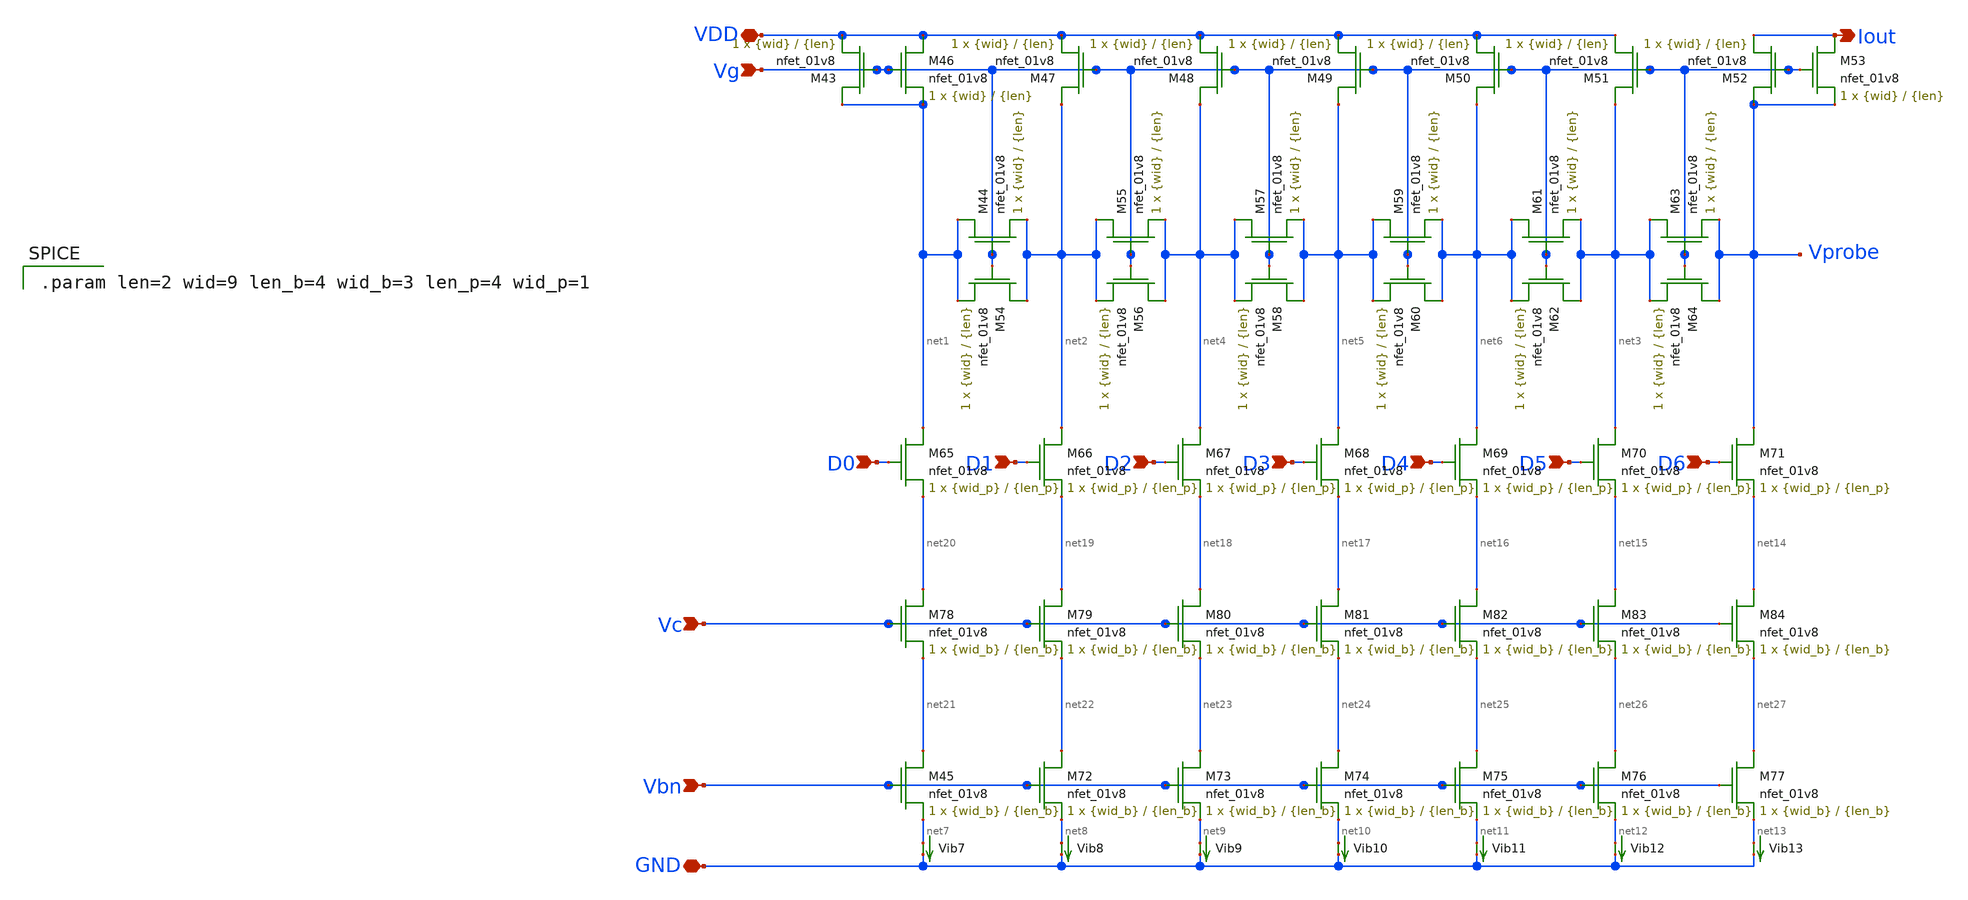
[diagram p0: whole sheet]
** sch_path: mp3/ladder.sch
**.subckt ladder Vbn VDD Iout GND D0 D1 D2 D3 D4 D5 D6 Vg Vc
*.ipin Vbn
*.iopin VDD
*.opin Iout
*.iopin GND
*.ipin D0
*.ipin D1
*.ipin D2
*.ipin D3
*.ipin D4
*.ipin D5
*.ipin D6
*.ipin Vg
*.ipin Vc
XM43 net1 Vg VDD GND sky130_fd_pr__nfet_01v8 L={len} W={wid} nf=1 ad='int((nf+1)/2) * W/nf * 0.29' as='int((nf+2)/2) * W/nf * 0.29'
+ pd='2*int((nf+1)/2) * (W/nf + 0.29)' ps='2*int((nf+2)/2) * (W/nf + 0.29)' nrd='0.29 / W' nrs='0.29 / W'
+ sa=0 sb=0 sd=0 mult=1 m=1
XM44 net1 Vg net2 GND sky130_fd_pr__nfet_01v8 L={len} W={wid} nf=1 ad='int((nf+1)/2) * W/nf * 0.29' as='int((nf+2)/2) * W/nf * 0.29'
+ pd='2*int((nf+1)/2) * (W/nf + 0.29)' ps='2*int((nf+2)/2) * (W/nf + 0.29)' nrd='0.29 / W' nrs='0.29 / W'
+ sa=0 sb=0 sd=0 mult=1 m=1
XM45 net21 Vbn net7 GND sky130_fd_pr__nfet_01v8 L={len_b} W={wid_b} nf=1 ad='int((nf+1)/2) * W/nf * 0.29'
+ as='int((nf+2)/2) * W/nf * 0.29' pd='2*int((nf+1)/2) * (W/nf + 0.29)' ps='2*int((nf+2)/2) * (W/nf + 0.29)'
+ nrd='0.29 / W' nrs='0.29 / W' sa=0 sb=0 sd=0 mult=1 m=1
XM46 VDD Vg net1 GND sky130_fd_pr__nfet_01v8 L={len} W={wid} nf=1 ad='int((nf+1)/2) * W/nf * 0.29' as='int((nf+2)/2) * W/nf * 0.29'
+ pd='2*int((nf+1)/2) * (W/nf + 0.29)' ps='2*int((nf+2)/2) * (W/nf + 0.29)' nrd='0.29 / W' nrs='0.29 / W'
+ sa=0 sb=0 sd=0 mult=1 m=1
XM47 net2 Vg VDD GND sky130_fd_pr__nfet_01v8 L={len} W={wid} nf=1 ad='int((nf+1)/2) * W/nf * 0.29' as='int((nf+2)/2) * W/nf * 0.29'
+ pd='2*int((nf+1)/2) * (W/nf + 0.29)' ps='2*int((nf+2)/2) * (W/nf + 0.29)' nrd='0.29 / W' nrs='0.29 / W'
+ sa=0 sb=0 sd=0 mult=1 m=1
XM48 net4 Vg VDD GND sky130_fd_pr__nfet_01v8 L={len} W={wid} nf=1 ad='int((nf+1)/2) * W/nf * 0.29' as='int((nf+2)/2) * W/nf * 0.29'
+ pd='2*int((nf+1)/2) * (W/nf + 0.29)' ps='2*int((nf+2)/2) * (W/nf + 0.29)' nrd='0.29 / W' nrs='0.29 / W'
+ sa=0 sb=0 sd=0 mult=1 m=1
XM49 net5 Vg VDD GND sky130_fd_pr__nfet_01v8 L={len} W={wid} nf=1 ad='int((nf+1)/2) * W/nf * 0.29' as='int((nf+2)/2) * W/nf * 0.29'
+ pd='2*int((nf+1)/2) * (W/nf + 0.29)' ps='2*int((nf+2)/2) * (W/nf + 0.29)' nrd='0.29 / W' nrs='0.29 / W'
+ sa=0 sb=0 sd=0 mult=1 m=1
XM50 net6 Vg VDD GND sky130_fd_pr__nfet_01v8 L={len} W={wid} nf=1 ad='int((nf+1)/2) * W/nf * 0.29' as='int((nf+2)/2) * W/nf * 0.29'
+ pd='2*int((nf+1)/2) * (W/nf + 0.29)' ps='2*int((nf+2)/2) * (W/nf + 0.29)' nrd='0.29 / W' nrs='0.29 / W'
+ sa=0 sb=0 sd=0 mult=1 m=1
XM51 net3 Vg VDD GND sky130_fd_pr__nfet_01v8 L={len} W={wid} nf=1 ad='int((nf+1)/2) * W/nf * 0.29' as='int((nf+2)/2) * W/nf * 0.29'
+ pd='2*int((nf+1)/2) * (W/nf + 0.29)' ps='2*int((nf+2)/2) * (W/nf + 0.29)' nrd='0.29 / W' nrs='0.29 / W'
+ sa=0 sb=0 sd=0 mult=1 m=1
XM52 Vprobe Vg Iout GND sky130_fd_pr__nfet_01v8 L={len} W={wid} nf=1 ad='int((nf+1)/2) * W/nf * 0.29'
+ as='int((nf+2)/2) * W/nf * 0.29' pd='2*int((nf+1)/2) * (W/nf + 0.29)' ps='2*int((nf+2)/2) * (W/nf + 0.29)'
+ nrd='0.29 / W' nrs='0.29 / W' sa=0 sb=0 sd=0 mult=1 m=1
XM53 Iout Vg Vprobe GND sky130_fd_pr__nfet_01v8 L={len} W={wid} nf=1 ad='int((nf+1)/2) * W/nf * 0.29'
+ as='int((nf+2)/2) * W/nf * 0.29' pd='2*int((nf+1)/2) * (W/nf + 0.29)' ps='2*int((nf+2)/2) * (W/nf + 0.29)'
+ nrd='0.29 / W' nrs='0.29 / W' sa=0 sb=0 sd=0 mult=1 m=1
XM54 net2 Vg net1 GND sky130_fd_pr__nfet_01v8 L={len} W={wid} nf=1 ad='int((nf+1)/2) * W/nf * 0.29' as='int((nf+2)/2) * W/nf * 0.29'
+ pd='2*int((nf+1)/2) * (W/nf + 0.29)' ps='2*int((nf+2)/2) * (W/nf + 0.29)' nrd='0.29 / W' nrs='0.29 / W'
+ sa=0 sb=0 sd=0 mult=1 m=1
XM55 net2 Vg net4 GND sky130_fd_pr__nfet_01v8 L={len} W={wid} nf=1 ad='int((nf+1)/2) * W/nf * 0.29' as='int((nf+2)/2) * W/nf * 0.29'
+ pd='2*int((nf+1)/2) * (W/nf + 0.29)' ps='2*int((nf+2)/2) * (W/nf + 0.29)' nrd='0.29 / W' nrs='0.29 / W'
+ sa=0 sb=0 sd=0 mult=1 m=1
XM56 net4 Vg net2 GND sky130_fd_pr__nfet_01v8 L={len} W={wid} nf=1 ad='int((nf+1)/2) * W/nf * 0.29' as='int((nf+2)/2) * W/nf * 0.29'
+ pd='2*int((nf+1)/2) * (W/nf + 0.29)' ps='2*int((nf+2)/2) * (W/nf + 0.29)' nrd='0.29 / W' nrs='0.29 / W'
+ sa=0 sb=0 sd=0 mult=1 m=1
XM57 net4 Vg net5 GND sky130_fd_pr__nfet_01v8 L={len} W={wid} nf=1 ad='int((nf+1)/2) * W/nf * 0.29' as='int((nf+2)/2) * W/nf * 0.29'
+ pd='2*int((nf+1)/2) * (W/nf + 0.29)' ps='2*int((nf+2)/2) * (W/nf + 0.29)' nrd='0.29 / W' nrs='0.29 / W'
+ sa=0 sb=0 sd=0 mult=1 m=1
XM58 net5 Vg net4 GND sky130_fd_pr__nfet_01v8 L={len} W={wid} nf=1 ad='int((nf+1)/2) * W/nf * 0.29' as='int((nf+2)/2) * W/nf * 0.29'
+ pd='2*int((nf+1)/2) * (W/nf + 0.29)' ps='2*int((nf+2)/2) * (W/nf + 0.29)' nrd='0.29 / W' nrs='0.29 / W'
+ sa=0 sb=0 sd=0 mult=1 m=1
XM59 net5 Vg net6 GND sky130_fd_pr__nfet_01v8 L={len} W={wid} nf=1 ad='int((nf+1)/2) * W/nf * 0.29' as='int((nf+2)/2) * W/nf * 0.29'
+ pd='2*int((nf+1)/2) * (W/nf + 0.29)' ps='2*int((nf+2)/2) * (W/nf + 0.29)' nrd='0.29 / W' nrs='0.29 / W'
+ sa=0 sb=0 sd=0 mult=1 m=1
XM60 net6 Vg net5 GND sky130_fd_pr__nfet_01v8 L={len} W={wid} nf=1 ad='int((nf+1)/2) * W/nf * 0.29' as='int((nf+2)/2) * W/nf * 0.29'
+ pd='2*int((nf+1)/2) * (W/nf + 0.29)' ps='2*int((nf+2)/2) * (W/nf + 0.29)' nrd='0.29 / W' nrs='0.29 / W'
+ sa=0 sb=0 sd=0 mult=1 m=1
XM61 net6 Vg net3 GND sky130_fd_pr__nfet_01v8 L={len} W={wid} nf=1 ad='int((nf+1)/2) * W/nf * 0.29' as='int((nf+2)/2) * W/nf * 0.29'
+ pd='2*int((nf+1)/2) * (W/nf + 0.29)' ps='2*int((nf+2)/2) * (W/nf + 0.29)' nrd='0.29 / W' nrs='0.29 / W'
+ sa=0 sb=0 sd=0 mult=1 m=1
XM62 net3 Vg net6 GND sky130_fd_pr__nfet_01v8 L={len} W={wid} nf=1 ad='int((nf+1)/2) * W/nf * 0.29' as='int((nf+2)/2) * W/nf * 0.29'
+ pd='2*int((nf+1)/2) * (W/nf + 0.29)' ps='2*int((nf+2)/2) * (W/nf + 0.29)' nrd='0.29 / W' nrs='0.29 / W'
+ sa=0 sb=0 sd=0 mult=1 m=1
XM63 net3 Vg Vprobe GND sky130_fd_pr__nfet_01v8 L={len} W={wid} nf=1 ad='int((nf+1)/2) * W/nf * 0.29'
+ as='int((nf+2)/2) * W/nf * 0.29' pd='2*int((nf+1)/2) * (W/nf + 0.29)' ps='2*int((nf+2)/2) * (W/nf + 0.29)'
+ nrd='0.29 / W' nrs='0.29 / W' sa=0 sb=0 sd=0 mult=1 m=1
XM64 Vprobe Vg net3 GND sky130_fd_pr__nfet_01v8 L={len} W={wid} nf=1 ad='int((nf+1)/2) * W/nf * 0.29'
+ as='int((nf+2)/2) * W/nf * 0.29' pd='2*int((nf+1)/2) * (W/nf + 0.29)' ps='2*int((nf+2)/2) * (W/nf + 0.29)'
+ nrd='0.29 / W' nrs='0.29 / W' sa=0 sb=0 sd=0 mult=1 m=1
Vib7 net7 GND 0
.save i(vib7)
Vib8 net8 GND 0
.save i(vib8)
Vib9 net9 GND 0
.save i(vib9)
Vib10 net10 GND 0
.save i(vib10)
Vib11 net11 GND 0
.save i(vib11)
Vib12 net12 GND 0
.save i(vib12)
Vib13 net13 GND 0
.save i(vib13)
XM65 net1 D0 net20 GND sky130_fd_pr__nfet_01v8 L={len_p} W={wid_p} nf=1 ad='int((nf+1)/2) * W/nf * 0.29'
+ as='int((nf+2)/2) * W/nf * 0.29' pd='2*int((nf+1)/2) * (W/nf + 0.29)' ps='2*int((nf+2)/2) * (W/nf + 0.29)'
+ nrd='0.29 / W' nrs='0.29 / W' sa=0 sb=0 sd=0 mult=1 m=1
XM66 net2 D1 net19 GND sky130_fd_pr__nfet_01v8 L={len_p} W={wid_p} nf=1 ad='int((nf+1)/2) * W/nf * 0.29'
+ as='int((nf+2)/2) * W/nf * 0.29' pd='2*int((nf+1)/2) * (W/nf + 0.29)' ps='2*int((nf+2)/2) * (W/nf + 0.29)'
+ nrd='0.29 / W' nrs='0.29 / W' sa=0 sb=0 sd=0 mult=1 m=1
XM67 net4 D2 net18 GND sky130_fd_pr__nfet_01v8 L={len_p} W={wid_p} nf=1 ad='int((nf+1)/2) * W/nf * 0.29'
+ as='int((nf+2)/2) * W/nf * 0.29' pd='2*int((nf+1)/2) * (W/nf + 0.29)' ps='2*int((nf+2)/2) * (W/nf + 0.29)'
+ nrd='0.29 / W' nrs='0.29 / W' sa=0 sb=0 sd=0 mult=1 m=1
XM68 net5 D3 net17 GND sky130_fd_pr__nfet_01v8 L={len_p} W={wid_p} nf=1 ad='int((nf+1)/2) * W/nf * 0.29'
+ as='int((nf+2)/2) * W/nf * 0.29' pd='2*int((nf+1)/2) * (W/nf + 0.29)' ps='2*int((nf+2)/2) * (W/nf + 0.29)'
+ nrd='0.29 / W' nrs='0.29 / W' sa=0 sb=0 sd=0 mult=1 m=1
XM69 net6 D4 net16 GND sky130_fd_pr__nfet_01v8 L={len_p} W={wid_p} nf=1 ad='int((nf+1)/2) * W/nf * 0.29'
+ as='int((nf+2)/2) * W/nf * 0.29' pd='2*int((nf+1)/2) * (W/nf + 0.29)' ps='2*int((nf+2)/2) * (W/nf + 0.29)'
+ nrd='0.29 / W' nrs='0.29 / W' sa=0 sb=0 sd=0 mult=1 m=1
XM70 net3 D5 net15 GND sky130_fd_pr__nfet_01v8 L={len_p} W={wid_p} nf=1 ad='int((nf+1)/2) * W/nf * 0.29'
+ as='int((nf+2)/2) * W/nf * 0.29' pd='2*int((nf+1)/2) * (W/nf + 0.29)' ps='2*int((nf+2)/2) * (W/nf + 0.29)'
+ nrd='0.29 / W' nrs='0.29 / W' sa=0 sb=0 sd=0 mult=1 m=1
XM71 Vprobe D6 net14 GND sky130_fd_pr__nfet_01v8 L={len_p} W={wid_p} nf=1 ad='int((nf+1)/2) * W/nf * 0.29'
+ as='int((nf+2)/2) * W/nf * 0.29' pd='2*int((nf+1)/2) * (W/nf + 0.29)' ps='2*int((nf+2)/2) * (W/nf + 0.29)'
+ nrd='0.29 / W' nrs='0.29 / W' sa=0 sb=0 sd=0 mult=1 m=1
XM72 net22 Vbn net8 GND sky130_fd_pr__nfet_01v8 L={len_b} W={wid_b} nf=1 ad='int((nf+1)/2) * W/nf * 0.29'
+ as='int((nf+2)/2) * W/nf * 0.29' pd='2*int((nf+1)/2) * (W/nf + 0.29)' ps='2*int((nf+2)/2) * (W/nf + 0.29)'
+ nrd='0.29 / W' nrs='0.29 / W' sa=0 sb=0 sd=0 mult=1 m=1
XM73 net23 Vbn net9 GND sky130_fd_pr__nfet_01v8 L={len_b} W={wid_b} nf=1 ad='int((nf+1)/2) * W/nf * 0.29'
+ as='int((nf+2)/2) * W/nf * 0.29' pd='2*int((nf+1)/2) * (W/nf + 0.29)' ps='2*int((nf+2)/2) * (W/nf + 0.29)'
+ nrd='0.29 / W' nrs='0.29 / W' sa=0 sb=0 sd=0 mult=1 m=1
XM74 net24 Vbn net10 GND sky130_fd_pr__nfet_01v8 L={len_b} W={wid_b} nf=1 ad='int((nf+1)/2) * W/nf * 0.29'
+ as='int((nf+2)/2) * W/nf * 0.29' pd='2*int((nf+1)/2) * (W/nf + 0.29)' ps='2*int((nf+2)/2) * (W/nf + 0.29)'
+ nrd='0.29 / W' nrs='0.29 / W' sa=0 sb=0 sd=0 mult=1 m=1
XM75 net25 Vbn net11 GND sky130_fd_pr__nfet_01v8 L={len_b} W={wid_b} nf=1 ad='int((nf+1)/2) * W/nf * 0.29'
+ as='int((nf+2)/2) * W/nf * 0.29' pd='2*int((nf+1)/2) * (W/nf + 0.29)' ps='2*int((nf+2)/2) * (W/nf + 0.29)'
+ nrd='0.29 / W' nrs='0.29 / W' sa=0 sb=0 sd=0 mult=1 m=1
XM76 net26 Vbn net12 GND sky130_fd_pr__nfet_01v8 L={len_b} W={wid_b} nf=1 ad='int((nf+1)/2) * W/nf * 0.29'
+ as='int((nf+2)/2) * W/nf * 0.29' pd='2*int((nf+1)/2) * (W/nf + 0.29)' ps='2*int((nf+2)/2) * (W/nf + 0.29)'
+ nrd='0.29 / W' nrs='0.29 / W' sa=0 sb=0 sd=0 mult=1 m=1
XM77 net27 Vbn net13 GND sky130_fd_pr__nfet_01v8 L={len_b} W={wid_b} nf=1 ad='int((nf+1)/2) * W/nf * 0.29'
+ as='int((nf+2)/2) * W/nf * 0.29' pd='2*int((nf+1)/2) * (W/nf + 0.29)' ps='2*int((nf+2)/2) * (W/nf + 0.29)'
+ nrd='0.29 / W' nrs='0.29 / W' sa=0 sb=0 sd=0 mult=1 m=1
XM78 net20 Vc net21 GND sky130_fd_pr__nfet_01v8 L={len_b} W={wid_b} nf=1 ad='int((nf+1)/2) * W/nf * 0.29'
+ as='int((nf+2)/2) * W/nf * 0.29' pd='2*int((nf+1)/2) * (W/nf + 0.29)' ps='2*int((nf+2)/2) * (W/nf + 0.29)'
+ nrd='0.29 / W' nrs='0.29 / W' sa=0 sb=0 sd=0 mult=1 m=1
XM79 net19 Vc net22 GND sky130_fd_pr__nfet_01v8 L={len_b} W={wid_b} nf=1 ad='int((nf+1)/2) * W/nf * 0.29'
+ as='int((nf+2)/2) * W/nf * 0.29' pd='2*int((nf+1)/2) * (W/nf + 0.29)' ps='2*int((nf+2)/2) * (W/nf + 0.29)'
+ nrd='0.29 / W' nrs='0.29 / W' sa=0 sb=0 sd=0 mult=1 m=1
XM80 net18 Vc net23 GND sky130_fd_pr__nfet_01v8 L={len_b} W={wid_b} nf=1 ad='int((nf+1)/2) * W/nf * 0.29'
+ as='int((nf+2)/2) * W/nf * 0.29' pd='2*int((nf+1)/2) * (W/nf + 0.29)' ps='2*int((nf+2)/2) * (W/nf + 0.29)'
+ nrd='0.29 / W' nrs='0.29 / W' sa=0 sb=0 sd=0 mult=1 m=1
XM81 net17 Vc net24 GND sky130_fd_pr__nfet_01v8 L={len_b} W={wid_b} nf=1 ad='int((nf+1)/2) * W/nf * 0.29'
+ as='int((nf+2)/2) * W/nf * 0.29' pd='2*int((nf+1)/2) * (W/nf + 0.29)' ps='2*int((nf+2)/2) * (W/nf + 0.29)'
+ nrd='0.29 / W' nrs='0.29 / W' sa=0 sb=0 sd=0 mult=1 m=1
XM82 net16 Vc net25 GND sky130_fd_pr__nfet_01v8 L={len_b} W={wid_b} nf=1 ad='int((nf+1)/2) * W/nf * 0.29'
+ as='int((nf+2)/2) * W/nf * 0.29' pd='2*int((nf+1)/2) * (W/nf + 0.29)' ps='2*int((nf+2)/2) * (W/nf + 0.29)'
+ nrd='0.29 / W' nrs='0.29 / W' sa=0 sb=0 sd=0 mult=1 m=1
XM83 net15 Vc net26 GND sky130_fd_pr__nfet_01v8 L={len_b} W={wid_b} nf=1 ad='int((nf+1)/2) * W/nf * 0.29'
+ as='int((nf+2)/2) * W/nf * 0.29' pd='2*int((nf+1)/2) * (W/nf + 0.29)' ps='2*int((nf+2)/2) * (W/nf + 0.29)'
+ nrd='0.29 / W' nrs='0.29 / W' sa=0 sb=0 sd=0 mult=1 m=1
XM84 net14 Vc net27 GND sky130_fd_pr__nfet_01v8 L={len_b} W={wid_b} nf=1 ad='int((nf+1)/2) * W/nf * 0.29'
+ as='int((nf+2)/2) * W/nf * 0.29' pd='2*int((nf+1)/2) * (W/nf + 0.29)' ps='2*int((nf+2)/2) * (W/nf + 0.29)'
+ nrd='0.29 / W' nrs='0.29 / W' sa=0 sb=0 sd=0 mult=1 m=1
**** begin user architecture code

.param len=2 wid=9 len_b=4 wid_b=3 len_p=4 wid_p=1

**** end user architecture code
**.ends
.end
